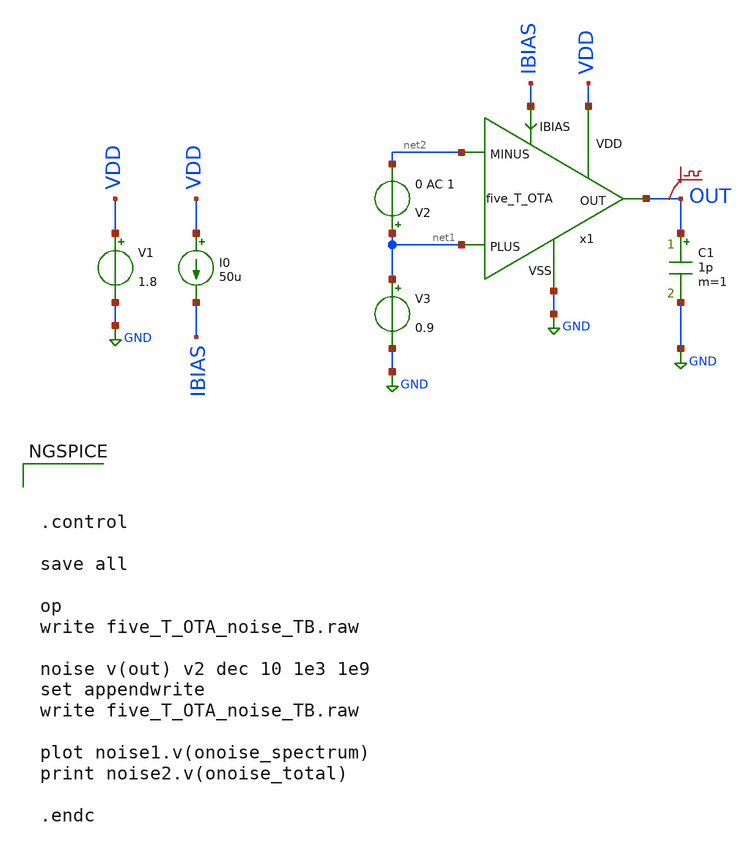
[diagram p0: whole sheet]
** sch_path: examples/xschem/five_T_OTA_noise_TB.sch
**.subckt five_T_OTA_noise_TB
x1 OUT net2 net1 IBIAS GND VDD five_T_OTA
V1 VDD GND 1.8
I0 VDD IBIAS 50u
V2 net1 net2 0 AC 1
V3 net1 GND 0.9
C1 OUT GND 1p m=1
.save v(out)
**** begin user architecture code



.control

save all

op
write five_T_OTA_noise_TB.raw

noise v(out) v2 dec 10 1e3 1e9
set appendwrite
write five_T_OTA_noise_TB.raw

plot noise1.v(onoise_spectrum)
print noise2.v(onoise_total)

.endc



** opencircuitdesign pdks install
.lib $::SKYWATER_MODELS/sky130.lib.spice tt


**** end user architecture code
**.ends

* expanding   symbol:  five_T_OTA.sym # of pins=6
** sym_path: examples/xschem/five_T_OTA.sym
** sch_path: examples/xschem/five_T_OTA.sch
.subckt five_T_OTA OUT MINUS PLUS IBIAS VSS VDD
*.iopin VDD
*.iopin VSS
*.iopin MINUS
*.iopin PLUS
*.iopin OUT
*.iopin IBIAS
XM2 IBIAS IBIAS VSS VSS sky130_fd_pr__nfet_01v8 L=0.3 W=3 nf=1 ad='int((nf+1)/2) * W/nf * 0.29' as='int((nf+2)/2) * W/nf * 0.29'
+ pd='2*int((nf+1)/2) * (W/nf + 0.29)' ps='2*int((nf+2)/2) * (W/nf + 0.29)' nrd='0.29 / W' nrs='0.29 / W'
+ sa=0 sb=0 sd=0 mult=1 m=1
XM1 net1 IBIAS VSS VSS sky130_fd_pr__nfet_01v8 L=0.3 W=3 nf=1 ad='int((nf+1)/2) * W/nf * 0.29' as='int((nf+2)/2) * W/nf * 0.29'
+ pd='2*int((nf+1)/2) * (W/nf + 0.29)' ps='2*int((nf+2)/2) * (W/nf + 0.29)' nrd='0.29 / W' nrs='0.29 / W'
+ sa=0 sb=0 sd=0 mult=4 m=4
.save v(ibias)
.save v(out)
.save v(net2)
.save v(net1)
XM4 net2 PLUS net1 VSS sky130_fd_pr__nfet_01v8_lvt L=0.3 W=4 nf=1 ad='int((nf+1)/2) * W/nf * 0.29' as='int((nf+2)/2) * W/nf * 0.29'
+ pd='2*int((nf+1)/2) * (W/nf + 0.29)' ps='2*int((nf+2)/2) * (W/nf + 0.29)' nrd='0.29 / W' nrs='0.29 / W'
+ sa=0 sb=0 sd=0 mult=4 m=4
XM5 OUT MINUS net1 VSS sky130_fd_pr__nfet_01v8_lvt L=0.3 W=4 nf=1 ad='int((nf+1)/2) * W/nf * 0.29' as='int((nf+2)/2) * W/nf * 0.29'
+ pd='2*int((nf+1)/2) * (W/nf + 0.29)' ps='2*int((nf+2)/2) * (W/nf + 0.29)' nrd='0.29 / W' nrs='0.29 / W'
+ sa=0 sb=0 sd=0 mult=4 m=4
XM3 net2 net2 VDD VDD sky130_fd_pr__pfet_01v8_lvt L=0.7 W=2.3 nf=1 ad='int((nf+1)/2) * W/nf * 0.29' as='int((nf+2)/2) * W/nf * 0.29'
+ pd='2*int((nf+1)/2) * (W/nf + 0.29)' ps='2*int((nf+2)/2) * (W/nf + 0.29)' nrd='0.29 / W' nrs='0.29 / W'
+ sa=0 sb=0 sd=0 mult=4 m=4
XM6 OUT net2 VDD VDD sky130_fd_pr__pfet_01v8_lvt L=0.7 W=2.3 nf=1 ad='int((nf+1)/2) * W/nf * 0.29' as='int((nf+2)/2) * W/nf * 0.29'
+ pd='2*int((nf+1)/2) * (W/nf + 0.29)' ps='2*int((nf+2)/2) * (W/nf + 0.29)' nrd='0.29 / W' nrs='0.29 / W'
+ sa=0 sb=0 sd=0 mult=4 m=4
.ends

.GLOBAL GND
.end
